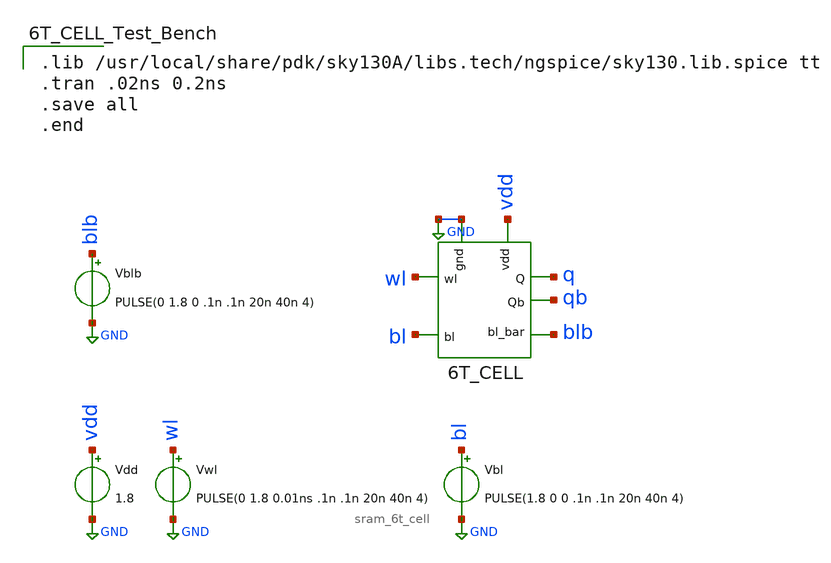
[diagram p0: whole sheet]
** sch_path: Projects/Schematic_Design_and_Analysis_of_an_8-Word_8-Bit_Static_RAM_with_6T_Storage_Cells_using_SKY130PDK/assets/schematic/sram_6tcell_tb.sch
**.subckt sram_6tcell_tb
x1 GND vdd wl bl blb q qb sram_6t_cell
Vdd vdd GND 1.8
Vwl wl GND PULSE(0 1.8 0.01ns .1n .1n 20n 40n 4)
Vbl bl GND PULSE(1.8 0 0 .1n .1n 20n 40n 4)
Vblb blb GND PULSE(0 1.8 0 .1n .1n 20n 40n 4)
**** begin user architecture code

.lib /usr/local/share/pdk/sky130A/libs.tech/ngspice/sky130.lib.spice tt
.tran .02ns 0.2ns
.save all
.end

**** end user architecture code
**.ends

* expanding   symbol:  sram_6t_cell.sym # of pins=7
** sym_path: Projects/Schematic_Design_and_Analysis_of_an_8-Word_8-Bit_Static_RAM_with_6T_Storage_Cells_using_SKY130PDK/assets/schematic/sram_6t_cell.sym
** sch_path: Projects/Schematic_Design_and_Analysis_of_an_8-Word_8-Bit_Static_RAM_with_6T_Storage_Cells_using_SKY130PDK/assets/schematic/sram_6t_cell.sch
.subckt sram_6t_cell gnd vdd wl bl bl_bar Q Qb
*.ipin gnd
*.ipin vdd
*.ipin bl_bar
*.ipin bl
*.ipin wl
*.opin Q
*.opin Qb
XM1 Qb Q gnd gnd sky130_fd_pr__nfet_01v8 L=0.15 W=2 nf=1 ad='int((nf+1)/2) * W/nf * 0.29' as='int((nf+2)/2) * W/nf * 0.29'
+ pd='2*int((nf+1)/2) * (W/nf + 0.29)' ps='2*int((nf+2)/2) * (W/nf + 0.29)' nrd='0.29 / W' nrs='0.29 / W'
+ sa=0 sb=0 sd=0 mult=1 m=1
XM2 Qb Q vdd vdd sky130_fd_pr__pfet_01v8 L=0.15 W=1 nf=1 ad='int((nf+1)/2) * W/nf * 0.29' as='int((nf+2)/2) * W/nf * 0.29'
+ pd='2*int((nf+1)/2) * (W/nf + 0.29)' ps='2*int((nf+2)/2) * (W/nf + 0.29)' nrd='0.29 / W' nrs='0.29 / W'
+ sa=0 sb=0 sd=0 mult=1 m=1
XM3 Q Qb gnd gnd sky130_fd_pr__nfet_01v8 L=0.15 W=2 nf=1 ad='int((nf+1)/2) * W/nf * 0.29' as='int((nf+2)/2) * W/nf * 0.29'
+ pd='2*int((nf+1)/2) * (W/nf + 0.29)' ps='2*int((nf+2)/2) * (W/nf + 0.29)' nrd='0.29 / W' nrs='0.29 / W'
+ sa=0 sb=0 sd=0 mult=1 m=1
XM4 Q Qb vdd vdd sky130_fd_pr__pfet_01v8 L=0.15 W=1 nf=1 ad='int((nf+1)/2) * W/nf * 0.29' as='int((nf+2)/2) * W/nf * 0.29'
+ pd='2*int((nf+1)/2) * (W/nf + 0.29)' ps='2*int((nf+2)/2) * (W/nf + 0.29)' nrd='0.29 / W' nrs='0.29 / W'
+ sa=0 sb=0 sd=0 mult=1 m=1
XM5 bl wl Q gnd sky130_fd_pr__nfet_01v8 L=0.15 W=1 nf=1 ad='int((nf+1)/2) * W/nf * 0.29' as='int((nf+2)/2) * W/nf * 0.29'
+ pd='2*int((nf+1)/2) * (W/nf + 0.29)' ps='2*int((nf+2)/2) * (W/nf + 0.29)' nrd='0.29 / W' nrs='0.29 / W'
+ sa=0 sb=0 sd=0 mult=1 m=1
XM6 bl_bar wl Qb gnd sky130_fd_pr__nfet_01v8 L=0.15 W=1 nf=1 ad='int((nf+1)/2) * W/nf * 0.29' as='int((nf+2)/2) * W/nf * 0.29'
+ pd='2*int((nf+1)/2) * (W/nf + 0.29)' ps='2*int((nf+2)/2) * (W/nf + 0.29)' nrd='0.29 / W' nrs='0.29 / W'
+ sa=0 sb=0 sd=0 mult=1 m=1
.ends

.GLOBAL GND
.end
